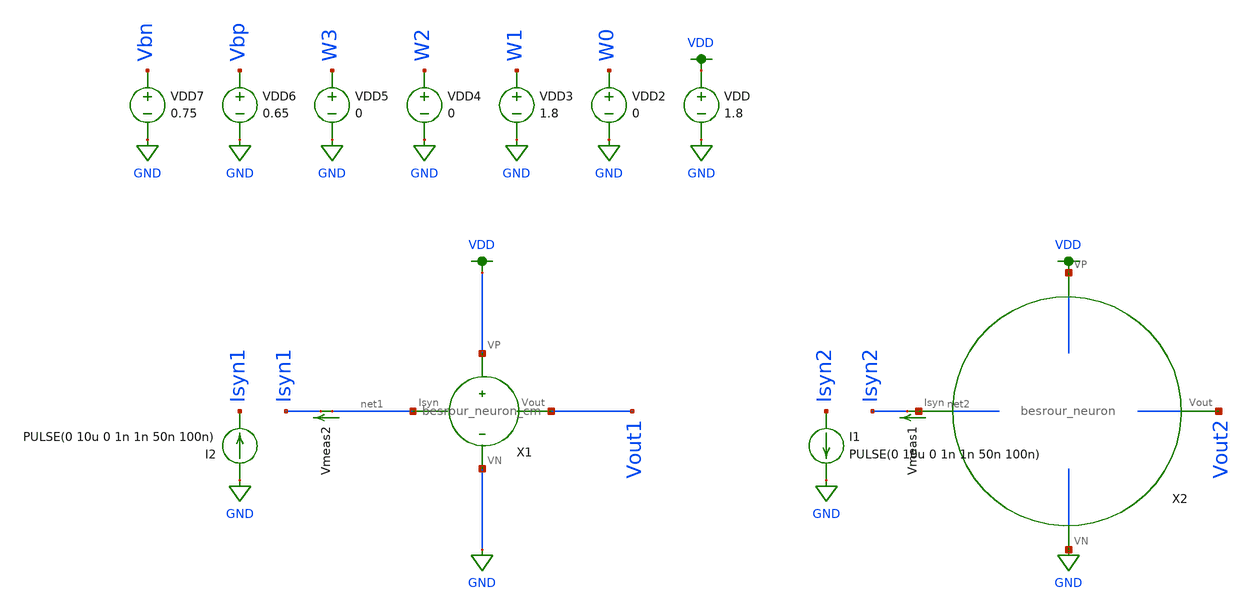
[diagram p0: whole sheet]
** sch_path: schematic/tran_neuron.sch
**.subckt tran_neuron
VDD VDD GND 1.8
VDD2 W0 GND 0
VDD3 W1 GND 1.8
VDD4 W2 GND 0
VDD5 W3 GND 0
VDD6 Vbp GND 0.65
VDD7 Vbn GND 0.75
I2 GND Isyn1 PULSE(0 10u 0 1n 1n 50n 100n)
Vmeas2 net1 Isyn1 0
.save i(vmeas2)
X1 net1 Vout1 VDD GND besrour_neuron_cm
I1 Isyn2 GND PULSE(0 10u 0 1n 1n 50n 100n)
Vmeas1 net2 Isyn2 0
.save i(vmeas1)
X2 net2 Vout2 VDD GND besrour_neuron
**** begin user architecture code

.param W=12
.param L=0.5
.tran 0.1n 250n
.save all


.option wnflag=1
.param MC_SWITCH=0.0
.lib ~/skywater/skywater-pdk/libraries/sky130_fd_pr_ngspice/latest/models/sky130.lib.spice tt

**** end user architecture code
**.ends

* expanding   symbol:  /home/madvlsi/neuromorphic_computing_final/schematic/besrour_neuron_cm.sym #
*+ of pins=4
** sym_path: schematic/besrour_neuron_cm.sym
** sch_path: schematic/besrour_neuron_cm.sch
.subckt besrour_neuron_cm Isyn Vout VP VN
*.iopin VP
*.iopin VN
*.iopin Isyn
*.opin Vout
XM2 VMEMINT net1 VP VDD sky130_fd_pr__pfet_01v8 L={L} W={W} nf=1 ad='int((nf+1)/2) * W/nf * 0.29' as='int((nf+2)/2) * W/nf * 0.29'
+ pd='2*int((nf+1)/2) * (W/nf + 0.29)' ps='2*int((nf+2)/2) * (W/nf + 0.29)' nrd='0.29 / W' nrs='0.29 / W'
+ sa=0 sb=0 sd=0 mult=1 m=1
XM3 VP net3 VMEMINT VDD sky130_fd_pr__pfet_01v8 L={L} W={W} nf=1 ad='int((nf+1)/2) * W/nf * 0.29' as='int((nf+2)/2) * W/nf * 0.29'
+ pd='2*int((nf+1)/2) * (W/nf + 0.29)' ps='2*int((nf+2)/2) * (W/nf + 0.29)' nrd='0.29 / W' nrs='0.29 / W'
+ sa=0 sb=0 sd=0 mult=1 m=1
XM4 net3 VMEMINT VP VDD sky130_fd_pr__pfet_01v8 L={L} W={W} nf=1 ad='int((nf+1)/2) * W/nf * 0.29' as='int((nf+2)/2) * W/nf * 0.29'
+ pd='2*int((nf+1)/2) * (W/nf + 0.29)' ps='2*int((nf+2)/2) * (W/nf + 0.29)' nrd='0.29 / W' nrs='0.29 / W'
+ sa=0 sb=0 sd=0 mult=1 m=1
XM5 net2 net3 VP VDD sky130_fd_pr__pfet_01v8 L={L} W={W} nf=1 ad='int((nf+1)/2) * W/nf * 0.29' as='int((nf+2)/2) * W/nf * 0.29'
+ pd='2*int((nf+1)/2) * (W/nf + 0.29)' ps='2*int((nf+2)/2) * (W/nf + 0.29)' nrd='0.29 / W' nrs='0.29 / W'
+ sa=0 sb=0 sd=0 mult=1 m=1
XM6 net3 VMEMINT VN GND sky130_fd_pr__nfet_01v8 L={L} W={W} nf=1 ad='int((nf+1)/2) * W/nf * 0.29' as='int((nf+2)/2) * W/nf * 0.29'
+ pd='2*int((nf+1)/2) * (W/nf + 0.29)' ps='2*int((nf+2)/2) * (W/nf + 0.29)' nrd='0.29 / W' nrs='0.29 / W'
+ sa=0 sb=0 sd=0 mult=1 m=1
XM8 net2 net3 VN GND sky130_fd_pr__nfet_01v8 L={L} W={W} nf=1 ad='int((nf+1)/2) * W/nf * 0.29' as='int((nf+2)/2) * W/nf * 0.29'
+ pd='2*int((nf+1)/2) * (W/nf + 0.29)' ps='2*int((nf+2)/2) * (W/nf + 0.29)' nrd='0.29 / W' nrs='0.29 / W'
+ sa=0 sb=0 sd=0 mult=1 m=1
C1 VMEMINT VN 340f m=1
C2 net2 VN 340f m=1
XM9 net4 net2 VP VDD sky130_fd_pr__pfet_01v8 L={L} W={W} nf=1 ad='int((nf+1)/2) * W/nf * 0.29' as='int((nf+2)/2) * W/nf * 0.29'
+ pd='2*int((nf+1)/2) * (W/nf + 0.29)' ps='2*int((nf+2)/2) * (W/nf + 0.29)' nrd='0.29 / W' nrs='0.29 / W'
+ sa=0 sb=0 sd=0 mult=1 m=1
XM10 net4 net2 VN GND sky130_fd_pr__nfet_01v8 L={L} W={W} nf=1 ad='int((nf+1)/2) * W/nf * 0.29' as='int((nf+2)/2) * W/nf * 0.29'
+ pd='2*int((nf+1)/2) * (W/nf + 0.29)' ps='2*int((nf+2)/2) * (W/nf + 0.29)' nrd='0.29 / W' nrs='0.29 / W'
+ sa=0 sb=0 sd=0 mult=1 m=1
XM11 Vout net4 VP VDD sky130_fd_pr__pfet_01v8 L={L} W={W} nf=1 ad='int((nf+1)/2) * W/nf * 0.29' as='int((nf+2)/2) * W/nf * 0.29'
+ pd='2*int((nf+1)/2) * (W/nf + 0.29)' ps='2*int((nf+2)/2) * (W/nf + 0.29)' nrd='0.29 / W' nrs='0.29 / W'
+ sa=0 sb=0 sd=0 mult=1 m=1
XM12 Vout net4 VN GND sky130_fd_pr__nfet_01v8 L={L} W={W} nf=1 ad='int((nf+1)/2) * W/nf * 0.29' as='int((nf+2)/2) * W/nf * 0.29'
+ pd='2*int((nf+1)/2) * (W/nf + 0.29)' ps='2*int((nf+2)/2) * (W/nf + 0.29)' nrd='0.29 / W' nrs='0.29 / W'
+ sa=0 sb=0 sd=0 mult=1 m=1
XM13 net1 Isyn VN GND sky130_fd_pr__nfet_01v8 L={L} W={W} nf=1 ad='int((nf+1)/2) * W/nf * 0.29' as='int((nf+2)/2) * W/nf * 0.29'
+ pd='2*int((nf+1)/2) * (W/nf + 0.29)' ps='2*int((nf+2)/2) * (W/nf + 0.29)' nrd='0.29 / W' nrs='0.29 / W'
+ sa=0 sb=0 sd=0 mult=1 m=1
XM14 VN Isyn Isyn GND sky130_fd_pr__nfet_01v8 L={L} W={W} nf=1 ad='int((nf+1)/2) * W/nf * 0.29' as='int((nf+2)/2) * W/nf * 0.29'
+ pd='2*int((nf+1)/2) * (W/nf + 0.29)' ps='2*int((nf+2)/2) * (W/nf + 0.29)' nrd='0.29 / W' nrs='0.29 / W'
+ sa=0 sb=0 sd=0 mult=1 m=1
XM1 VP net1 net1 VDD sky130_fd_pr__pfet_01v8 L={L} W={W} nf=1 ad='int((nf+1)/2) * W/nf * 0.29' as='int((nf+2)/2) * W/nf * 0.29'
+ pd='2*int((nf+1)/2) * (W/nf + 0.29)' ps='2*int((nf+2)/2) * (W/nf + 0.29)' nrd='0.29 / W' nrs='0.29 / W'
+ sa=0 sb=0 sd=0 mult=1 m=1
XM7 VN net2 VMEMINT GND sky130_fd_pr__nfet_01v8 L={L} W={W} nf=1 ad='int((nf+1)/2) * W/nf * 0.29' as='int((nf+2)/2) * W/nf * 0.29'
+ pd='2*int((nf+1)/2) * (W/nf + 0.29)' ps='2*int((nf+2)/2) * (W/nf + 0.29)' nrd='0.29 / W' nrs='0.29 / W'
+ sa=0 sb=0 sd=0 mult=1 m=1
.ends


* expanding   symbol:  /home/madvlsi/neuromorphic_computing_final/schematic/besrour_neuron.sym # of
*+ pins=4
** sym_path: schematic/besrour_neuron.sym
** sch_path: schematic/besrour_neuron.sch
.subckt besrour_neuron Isyn Vout VP VN
*.opin Vout
*.iopin VP
*.iopin VN
*.iopin Isyn
XM1 VP Isyn Isyn VDD sky130_fd_pr__pfet_01v8 L={L} W={W} nf=1 ad='int((nf+1)/2) * W/nf * 0.29' as='int((nf+2)/2) * W/nf * 0.29'
+ pd='2*int((nf+1)/2) * (W/nf + 0.29)' ps='2*int((nf+2)/2) * (W/nf + 0.29)' nrd='0.29 / W' nrs='0.29 / W'
+ sa=0 sb=0 sd=0 mult=1 m=1
XM7 VN Vout VMEMINT GND sky130_fd_pr__nfet_01v8 L={L} W={W} nf=1 ad='int((nf+1)/2) * W/nf * 0.29' as='int((nf+2)/2) * W/nf * 0.29'
+ pd='2*int((nf+1)/2) * (W/nf + 0.29)' ps='2*int((nf+2)/2) * (W/nf + 0.29)' nrd='0.29 / W' nrs='0.29 / W'
+ sa=0 sb=0 sd=0 mult=1 m=1
XM2 VMEMINT Isyn VP VDD sky130_fd_pr__pfet_01v8 L={L} W={W} nf=1 ad='int((nf+1)/2) * W/nf * 0.29' as='int((nf+2)/2) * W/nf * 0.29'
+ pd='2*int((nf+1)/2) * (W/nf + 0.29)' ps='2*int((nf+2)/2) * (W/nf + 0.29)' nrd='0.29 / W' nrs='0.29 / W'
+ sa=0 sb=0 sd=0 mult=1 m=1
XM3 VP net1 VMEMINT VDD sky130_fd_pr__pfet_01v8 L={L} W={W} nf=1 ad='int((nf+1)/2) * W/nf * 0.29' as='int((nf+2)/2) * W/nf * 0.29'
+ pd='2*int((nf+1)/2) * (W/nf + 0.29)' ps='2*int((nf+2)/2) * (W/nf + 0.29)' nrd='0.29 / W' nrs='0.29 / W'
+ sa=0 sb=0 sd=0 mult=1 m=1
XM4 net1 VMEMINT VP VDD sky130_fd_pr__pfet_01v8 L={L} W={W} nf=1 ad='int((nf+1)/2) * W/nf * 0.29' as='int((nf+2)/2) * W/nf * 0.29'
+ pd='2*int((nf+1)/2) * (W/nf + 0.29)' ps='2*int((nf+2)/2) * (W/nf + 0.29)' nrd='0.29 / W' nrs='0.29 / W'
+ sa=0 sb=0 sd=0 mult=1 m=1
XM5 Vout net1 VP VDD sky130_fd_pr__pfet_01v8 L={L} W={W} nf=1 ad='int((nf+1)/2) * W/nf * 0.29' as='int((nf+2)/2) * W/nf * 0.29'
+ pd='2*int((nf+1)/2) * (W/nf + 0.29)' ps='2*int((nf+2)/2) * (W/nf + 0.29)' nrd='0.29 / W' nrs='0.29 / W'
+ sa=0 sb=0 sd=0 mult=1 m=1
XM6 net1 VMEMINT VN GND sky130_fd_pr__nfet_01v8 L={L} W={W} nf=1 ad='int((nf+1)/2) * W/nf * 0.29' as='int((nf+2)/2) * W/nf * 0.29'
+ pd='2*int((nf+1)/2) * (W/nf + 0.29)' ps='2*int((nf+2)/2) * (W/nf + 0.29)' nrd='0.29 / W' nrs='0.29 / W'
+ sa=0 sb=0 sd=0 mult=1 m=1
XM8 Vout net1 VN GND sky130_fd_pr__nfet_01v8 L={L} W={W} nf=1 ad='int((nf+1)/2) * W/nf * 0.29' as='int((nf+2)/2) * W/nf * 0.29'
+ pd='2*int((nf+1)/2) * (W/nf + 0.29)' ps='2*int((nf+2)/2) * (W/nf + 0.29)' nrd='0.29 / W' nrs='0.29 / W'
+ sa=0 sb=0 sd=0 mult=1 m=1
C1 VMEMINT VN 34f m=1
C2 Vout VN 34f m=1
.ends

.GLOBAL GND
.GLOBAL VDD
.end
